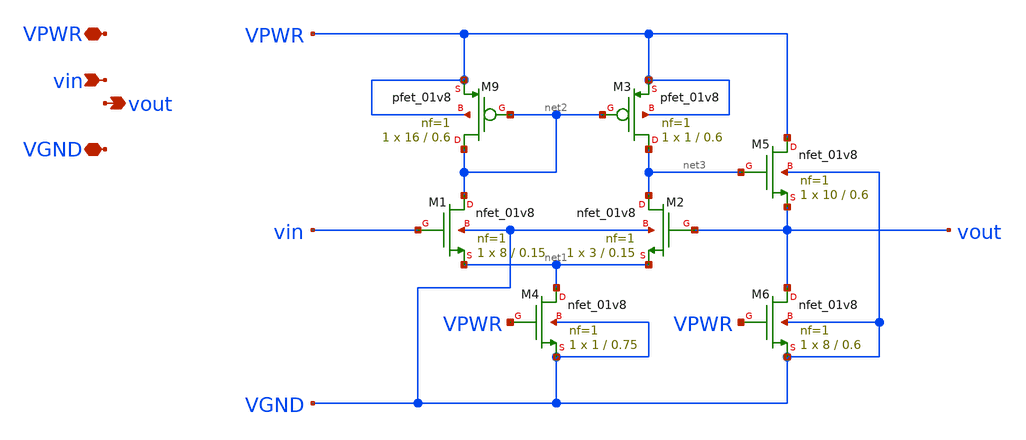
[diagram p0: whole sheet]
** sch_path: xschem/vbuff.sch
**.subckt vbuff VPWR vin vout VGND
*.iopin VPWR
*.ipin vin
*.opin vout
*.iopin VGND
XM1 net2 vin net1 VGND sky130_fd_pr__nfet_01v8 L=0.15 W=8 nf=1 ad='int((nf+1)/2) * W/nf * 0.29' as='int((nf+2)/2) * W/nf * 0.29'
+ pd='2*int((nf+1)/2) * (W/nf + 0.29)' ps='2*int((nf+2)/2) * (W/nf + 0.29)' nrd='0.29 / W' nrs='0.29 / W'
+ sa=0 sb=0 sd=0 mult=1 m=1
XM9 net2 net2 VPWR VPWR sky130_fd_pr__pfet_01v8 L=0.6 W=16 nf=1 ad='int((nf+1)/2) * W/nf * 0.29' as='int((nf+2)/2) * W/nf * 0.29'
+ pd='2*int((nf+1)/2) * (W/nf + 0.29)' ps='2*int((nf+2)/2) * (W/nf + 0.29)' nrd='0.29 / W' nrs='0.29 / W'
+ sa=0 sb=0 sd=0 mult=1 m=1
XM2 net3 vout net1 VGND sky130_fd_pr__nfet_01v8 L=0.15 W=3 nf=1 ad='int((nf+1)/2) * W/nf * 0.29' as='int((nf+2)/2) * W/nf * 0.29'
+ pd='2*int((nf+1)/2) * (W/nf + 0.29)' ps='2*int((nf+2)/2) * (W/nf + 0.29)' nrd='0.29 / W' nrs='0.29 / W'
+ sa=0 sb=0 sd=0 mult=1 m=1
XM3 net3 net2 VPWR VPWR sky130_fd_pr__pfet_01v8 L=0.6 W=1 nf=1 ad='int((nf+1)/2) * W/nf * 0.29' as='int((nf+2)/2) * W/nf * 0.29'
+ pd='2*int((nf+1)/2) * (W/nf + 0.29)' ps='2*int((nf+2)/2) * (W/nf + 0.29)' nrd='0.29 / W' nrs='0.29 / W'
+ sa=0 sb=0 sd=0 mult=1 m=1
XM4 net1 VPWR VGND VGND sky130_fd_pr__nfet_01v8 L=0.75 W=1 nf=1 ad='int((nf+1)/2) * W/nf * 0.29' as='int((nf+2)/2) * W/nf * 0.29'
+ pd='2*int((nf+1)/2) * (W/nf + 0.29)' ps='2*int((nf+2)/2) * (W/nf + 0.29)' nrd='0.29 / W' nrs='0.29 / W'
+ sa=0 sb=0 sd=0 mult=1 m=1
XM5 VPWR net3 vout VGND sky130_fd_pr__nfet_01v8 L=0.6 W=10 nf=1 ad='int((nf+1)/2) * W/nf * 0.29' as='int((nf+2)/2) * W/nf * 0.29'
+ pd='2*int((nf+1)/2) * (W/nf + 0.29)' ps='2*int((nf+2)/2) * (W/nf + 0.29)' nrd='0.29 / W' nrs='0.29 / W'
+ sa=0 sb=0 sd=0 mult=1 m=1
XM6 vout VPWR VGND VGND sky130_fd_pr__nfet_01v8 L=0.6 W=8 nf=1 ad='int((nf+1)/2) * W/nf * 0.29' as='int((nf+2)/2) * W/nf * 0.29'
+ pd='2*int((nf+1)/2) * (W/nf + 0.29)' ps='2*int((nf+2)/2) * (W/nf + 0.29)' nrd='0.29 / W' nrs='0.29 / W'
+ sa=0 sb=0 sd=0 mult=1 m=1
**.ends
.end
